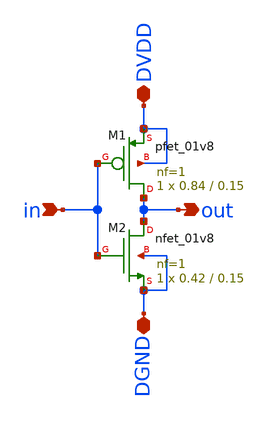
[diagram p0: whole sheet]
** sch_path: tutorial-6/source/inv.sch
**.subckt inv DVDD DGND in out
*.iopin DVDD
*.iopin DGND
*.ipin in
*.opin out
XM1 out in DVDD DVDD sky130_fd_pr__pfet_01v8 L=0.15 W=0.84 nf=1 ad='int((nf+1)/2) * W/nf * 0.29' as='int((nf+2)/2) * W/nf * 0.29'
+ pd='2*int((nf+1)/2) * (W/nf + 0.29)' ps='2*int((nf+2)/2) * (W/nf + 0.29)' nrd='0.29 / W' nrs='0.29 / W'
+ sa=0 sb=0 sd=0 mult=1 m=1
XM2 out in DGND DGND sky130_fd_pr__nfet_01v8 L=0.15 W=0.42 nf=1 ad='int((nf+1)/2) * W/nf * 0.29' as='int((nf+2)/2) * W/nf * 0.29'
+ pd='2*int((nf+1)/2) * (W/nf + 0.29)' ps='2*int((nf+2)/2) * (W/nf + 0.29)' nrd='0.29 / W' nrs='0.29 / W'
+ sa=0 sb=0 sd=0 mult=1 m=1
**.ends
.end
